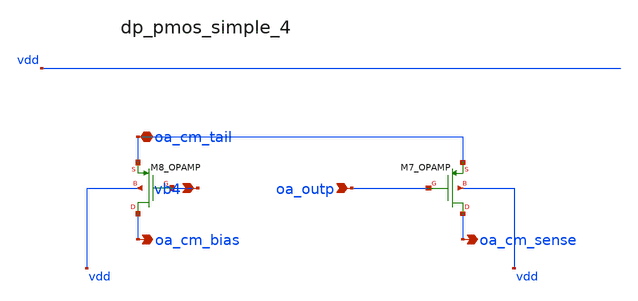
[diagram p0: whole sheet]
** sch_path: analog-db/raw/sup_003_rrl_sc_integrator/hier/blocks/dp_pmos_simple_4.sch
**.subckt dp_pmos_simple_4 vb4 oa_outp oa_cm_tail oa_cm_bias oa_cm_sense
*.ipin vb4
*.ipin oa_outp
*.iopin oa_cm_tail
*.opin oa_cm_bias
*.opin oa_cm_sense
XM7_OPAMP oa_cm_sense oa_outp oa_cm_tail vdd sg13_lv_pmos w=x_dut_xm7_opamp_w l=x_dut_xm7_opamp_l
+ ng=1 m=x_dut_xm7_opamp_m
XM8_OPAMP oa_cm_bias vb4 oa_cm_tail vdd sg13_lv_pmos w=x_dut_xm8_opamp_w l=x_dut_xm8_opamp_l ng=1
+ m=x_dut_xm8_opamp_m
**.ends
.end
